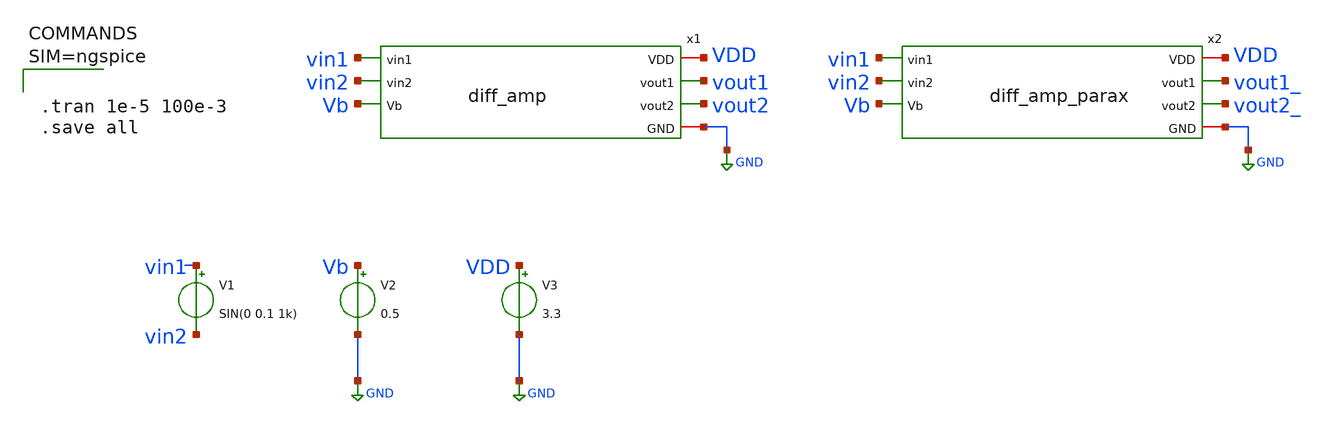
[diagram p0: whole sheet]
** sch_path: xschem/differential_amplifier.sch
**.subckt differential_amplifier
V1 vin1 vin2 SIN(0 0.1 1k)
V2 Vb GND 0.5
V3 VDD GND 3.3
x1 VDD vout1 vout2 vin1 vin2 Vb GND diff_amp
x2 VDD vout1_ vout2_ vin1 vin2 Vb GND diff_amp_parax
**** begin user architecture code



.tran 1e-5 100e-3
.save all





.lib /usr/local/share/pdk/sky130A/libs.tech/ngspice/sky130.lib.spice tt
.include /usr/local/share/pdk/sky130A/libs.ref/sky130_fd_sc_hd/spice/sky130_fd_sc_hd.spice


**** end user architecture code
**.ends

* expanding   symbol:  diff_amp.sym # of pins=7
** sym_path: xschem/diff_amp.sym
** sch_path: xschem/diff_amp.sch
.subckt diff_amp VDD vout1 vout2 vin1 vin2 Vb GND
*.ipin Vb
*.opin vout2
*.opin vout1
*.ipin vin2
*.ipin vin1
*.iopin GND
*.iopin VDD
XM1 virtual_gnd Vb GND GND sky130_fd_pr__nfet_01v8 L=0.15 W=10 nf=1 ad='int((nf+1)/2) * W/nf * 0.29'
+ as='int((nf+2)/2) * W/nf * 0.29' pd='2*int((nf+1)/2) * (W/nf + 0.29)' ps='2*int((nf+2)/2) * (W/nf + 0.29)'
+ nrd='0.29 / W' nrs='0.29 / W' sa=0 sb=0 sd=0 mult=1 m=1
XM2 vout1 vout1 VDD VDD sky130_fd_pr__pfet_01v8 L=0.15 W=2 nf=1 ad='int((nf+1)/2) * W/nf * 0.29' as='int((nf+2)/2) * W/nf * 0.29'
+ pd='2*int((nf+1)/2) * (W/nf + 0.29)' ps='2*int((nf+2)/2) * (W/nf + 0.29)' nrd='0.29 / W' nrs='0.29 / W'
+ sa=0 sb=0 sd=0 mult=1 m=1
XM3 vout2 vout2 VDD VDD sky130_fd_pr__pfet_01v8 L=0.15 W=2 nf=1 ad='int((nf+1)/2) * W/nf * 0.29' as='int((nf+2)/2) * W/nf * 0.29'
+ pd='2*int((nf+1)/2) * (W/nf + 0.29)' ps='2*int((nf+2)/2) * (W/nf + 0.29)' nrd='0.29 / W' nrs='0.29 / W'
+ sa=0 sb=0 sd=0 mult=1 m=1
XM4 vout1 vin1 virtual_gnd GND sky130_fd_pr__nfet_01v8 L=0.15 W=1 nf=1 ad='int((nf+1)/2) * W/nf * 0.29'
+ as='int((nf+2)/2) * W/nf * 0.29' pd='2*int((nf+1)/2) * (W/nf + 0.29)' ps='2*int((nf+2)/2) * (W/nf + 0.29)'
+ nrd='0.29 / W' nrs='0.29 / W' sa=0 sb=0 sd=0 mult=1 m=1
XM5 vout2 vin2 virtual_gnd GND sky130_fd_pr__nfet_01v8 L=0.15 W=1 nf=1 ad='int((nf+1)/2) * W/nf * 0.29'
+ as='int((nf+2)/2) * W/nf * 0.29' pd='2*int((nf+1)/2) * (W/nf + 0.29)' ps='2*int((nf+2)/2) * (W/nf + 0.29)'
+ nrd='0.29 / W' nrs='0.29 / W' sa=0 sb=0 sd=0 mult=1 m=1
.ends


* expanding   symbol:  diff_amp_parax.sym # of pins=7
** sym_path: xschem/diff_amp.sym
.include [file normalize ../mag/diff_amp.sim.spice]
.GLOBAL GND
.end
